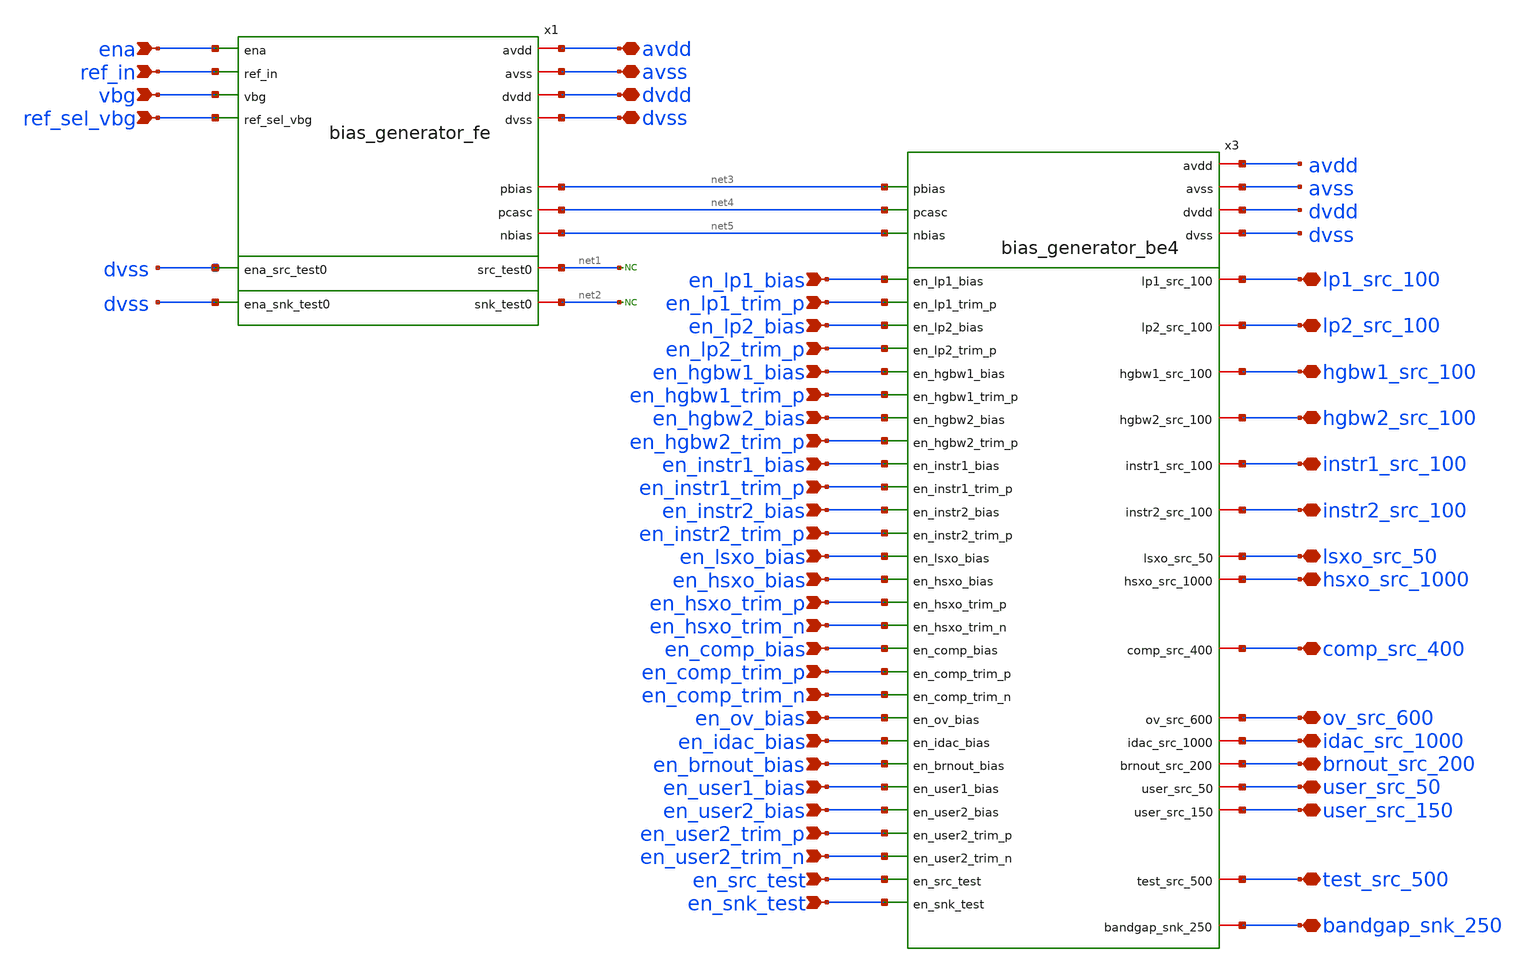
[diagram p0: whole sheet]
** sch_path: xschem/sky130_ef_ip__biasgen4.sch
**.subckt sky130_ef_ip__biasgen4 avdd avss dvdd dvss lp1_src_100 lp2_src_100 hgbw1_src_100
*+ hgbw2_src_100 instr1_src_100 instr2_src_100 lsxo_src_50 hsxo_src_1000 comp_src_400 ov_src_600 idac_src_1000
*+ brnout_src_200 user_src_50 user_src_150 test_src_500 ena ref_in vbg ref_sel_vbg en_lp1_bias en_lp1_trim_p
*+ en_lp2_bias en_lp2_trim_p en_hgbw1_bias en_hgbw1_trim_p en_hgbw2_bias en_hgbw2_trim_p en_instr1_bias
*+ en_instr2_bias en_instr1_trim_p en_instr2_trim_p en_lsxo_bias en_hsxo_bias en_hsxo_trim_p en_hsxo_trim_n
*+ en_comp_bias en_comp_trim_p en_comp_trim_n en_ov_bias en_idac_bias en_brnout_bias en_user1_bias en_user2_bias
*+ en_user2_trim_p en_user2_trim_n en_src_test en_snk_test bandgap_snk_250
*.iopin avdd
*.iopin avss
*.iopin dvdd
*.iopin dvss
*.iopin lp1_src_100
*.iopin lp2_src_100
*.iopin hgbw1_src_100
*.iopin hgbw2_src_100
*.iopin instr1_src_100
*.iopin instr2_src_100
*.iopin lsxo_src_50
*.iopin hsxo_src_1000
*.iopin comp_src_400
*.iopin ov_src_600
*.iopin idac_src_1000
*.iopin brnout_src_200
*.iopin user_src_50
*.iopin user_src_150
*.iopin test_src_500
*.ipin ena
*.ipin ref_in
*.ipin vbg
*.ipin ref_sel_vbg
*.ipin en_lp1_bias
*.ipin en_lp1_trim_p
*.ipin en_lp2_bias
*.ipin en_lp2_trim_p
*.ipin en_hgbw1_bias
*.ipin en_hgbw1_trim_p
*.ipin en_hgbw2_bias
*.ipin en_hgbw2_trim_p
*.ipin en_instr1_bias
*.ipin en_instr2_bias
*.ipin en_instr1_trim_p
*.ipin en_instr2_trim_p
*.ipin en_lsxo_bias
*.ipin en_hsxo_bias
*.ipin en_hsxo_trim_p
*.ipin en_hsxo_trim_n
*.ipin en_comp_bias
*.ipin en_comp_trim_p
*.ipin en_comp_trim_n
*.ipin en_ov_bias
*.ipin en_idac_bias
*.ipin en_brnout_bias
*.ipin en_user1_bias
*.ipin en_user2_bias
*.ipin en_user2_trim_p
*.ipin en_user2_trim_n
*.ipin en_src_test
*.ipin en_snk_test
*.iopin bandgap_snk_250
x1 avdd ena vbg net1 avss dvdd dvss ref_sel_vbg ref_in dvss net5 net4 net3 net2 dvss
+ bias_generator_fe
* noconn #net1
* noconn #net2
x3 dvdd dvss en_hsxo_bias en_comp_trim_n en_ov_bias avdd en_comp_bias net4 en_hsxo_trim_n net3
+ en_lp1_bias en_user2_trim_n en_lp2_bias en_hgbw1_bias lp1_src_100 test_src_500 lp2_src_100 en_hgbw2_bias
+ user_src_50 idac_src_1000 lsxo_src_50 hsxo_src_1000 comp_src_400 hgbw2_src_100 ov_src_600 user_src_150
+ instr1_src_100 instr2_src_100 hgbw1_src_100 en_instr1_bias en_instr2_bias en_src_test en_lsxo_bias en_snk_test
+ net5 en_user1_bias avss en_idac_bias en_user2_bias en_comp_trim_p en_hsxo_trim_p en_user2_trim_p
+ en_lp1_trim_p en_lp2_trim_p en_hgbw1_trim_p en_hgbw2_trim_p en_instr1_trim_p en_instr2_trim_p brnout_src_200
+ en_brnout_bias bandgap_snk_250 bias_generator_be4
**.ends
.end
